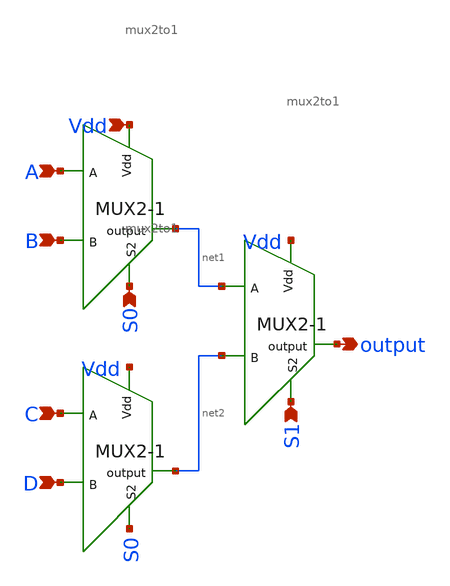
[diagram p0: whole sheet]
** sch_path: extra_stuff/mux4to1.sch
**.subckt mux4to1 output S1 S0 A B C D Vdd
*.opin output
*.ipin S1
*.ipin S0
*.ipin A
*.ipin B
*.ipin C
*.ipin D
*.ipin Vdd
x2 output Vdd net1 net2 S1 mux2to1
x4 net1 Vdd A B S0 mux2to1
x5 net2 Vdd C D S0 mux2to1
**.ends
.end
